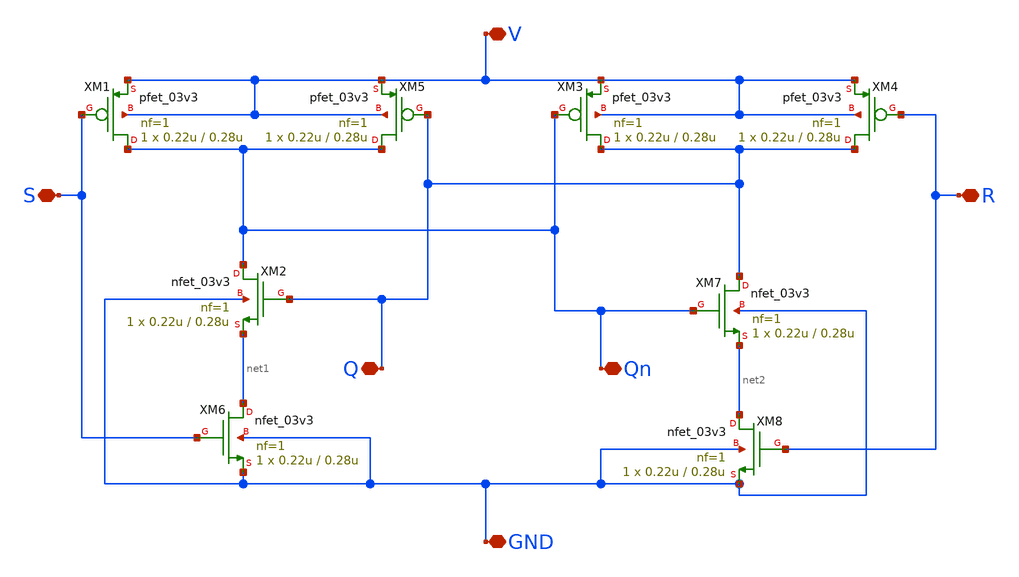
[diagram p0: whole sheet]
** sch_path: V2/Simbolos/SR_nand.sch
**.subckt SR_nand S R V GND Qn Q
*.iopin S
*.iopin R
*.iopin V
*.iopin GND
*.iopin Qn
*.iopin Q
XM1 Qn S V V pfet_03v3 L=0.28u W=0.22u nf=1 ad='int((nf+1)/2) * W/nf * 0.18u' as='int((nf+2)/2) * W/nf * 0.18u'
+ pd='2*int((nf+1)/2) * (W/nf + 0.18u)' ps='2*int((nf+2)/2) * (W/nf + 0.18u)' nrd='0.18u / W' nrs='0.18u / W'
+ sa=0 sb=0 sd=0 m=1
XM2 Qn Q net1 GND nfet_03v3 L=0.28u W=0.22u nf=1 ad='int((nf+1)/2) * W/nf * 0.18u' as='int((nf+2)/2) * W/nf * 0.18u'
+ pd='2*int((nf+1)/2) * (W/nf + 0.18u)' ps='2*int((nf+2)/2) * (W/nf + 0.18u)' nrd='0.18u / W' nrs='0.18u / W'
+ sa=0 sb=0 sd=0 m=1
XM3 Q Qn V V pfet_03v3 L=0.28u W=0.22u nf=1 ad='int((nf+1)/2) * W/nf * 0.18u' as='int((nf+2)/2) * W/nf * 0.18u'
+ pd='2*int((nf+1)/2) * (W/nf + 0.18u)' ps='2*int((nf+2)/2) * (W/nf + 0.18u)' nrd='0.18u / W' nrs='0.18u / W'
+ sa=0 sb=0 sd=0 m=1
XM4 Q R V V pfet_03v3 L=0.28u W=0.22u nf=1 ad='int((nf+1)/2) * W/nf * 0.18u' as='int((nf+2)/2) * W/nf * 0.18u'
+ pd='2*int((nf+1)/2) * (W/nf + 0.18u)' ps='2*int((nf+2)/2) * (W/nf + 0.18u)' nrd='0.18u / W' nrs='0.18u / W'
+ sa=0 sb=0 sd=0 m=1
XM5 Qn Q V V pfet_03v3 L=0.28u W=0.22u nf=1 ad='int((nf+1)/2) * W/nf * 0.18u' as='int((nf+2)/2) * W/nf * 0.18u'
+ pd='2*int((nf+1)/2) * (W/nf + 0.18u)' ps='2*int((nf+2)/2) * (W/nf + 0.18u)' nrd='0.18u / W' nrs='0.18u / W'
+ sa=0 sb=0 sd=0 m=1
XM6 net1 S GND GND nfet_03v3 L=0.28u W=0.22u nf=1 ad='int((nf+1)/2) * W/nf * 0.18u' as='int((nf+2)/2) * W/nf * 0.18u'
+ pd='2*int((nf+1)/2) * (W/nf + 0.18u)' ps='2*int((nf+2)/2) * (W/nf + 0.18u)' nrd='0.18u / W' nrs='0.18u / W'
+ sa=0 sb=0 sd=0 m=1
XM7 Q Qn net2 GND nfet_03v3 L=0.28u W=0.22u nf=1 ad='int((nf+1)/2) * W/nf * 0.18u' as='int((nf+2)/2) * W/nf * 0.18u'
+ pd='2*int((nf+1)/2) * (W/nf + 0.18u)' ps='2*int((nf+2)/2) * (W/nf + 0.18u)' nrd='0.18u / W' nrs='0.18u / W'
+ sa=0 sb=0 sd=0 m=1
XM8 net2 R GND GND nfet_03v3 L=0.28u W=0.22u nf=1 ad='int((nf+1)/2) * W/nf * 0.18u' as='int((nf+2)/2) * W/nf * 0.18u'
+ pd='2*int((nf+1)/2) * (W/nf + 0.18u)' ps='2*int((nf+2)/2) * (W/nf + 0.18u)' nrd='0.18u / W' nrs='0.18u / W'
+ sa=0 sb=0 sd=0 m=1
**** begin user architecture code

.include /foss/pdks/gf180mcuC/libs.tech/ngspice/design.ngspice
.lib /foss/pdks/gf180mcuC/libs.tech/ngspice/sm141064.ngspice typical

**** end user architecture code
**.ends
.end
